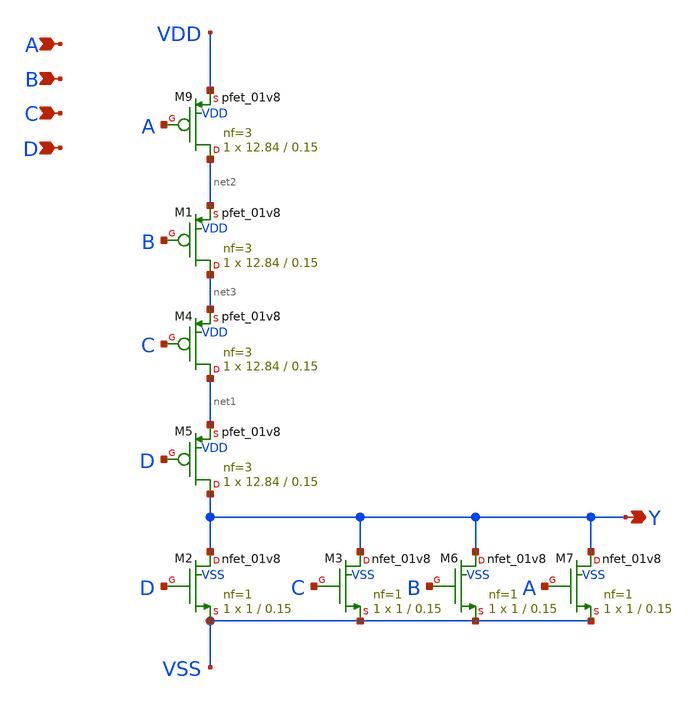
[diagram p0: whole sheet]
** sch_path: design/xschem/NOR/nor4.sch
**.subckt nor4 Y B C A D
*.opin Y
*.ipin B
*.ipin C
*.ipin A
*.ipin D
XM2 Y D VSS VSS sky130_fd_pr__nfet_01v8 L=0.15 W=1 nf=1 ad='int((nf+1)/2) * W/nf * 0.29' as='int((nf+2)/2) * W/nf * 0.29'
+ pd='2*int((nf+1)/2) * (W/nf + 0.29)' ps='2*int((nf+2)/2) * (W/nf + 0.29)' nrd='0.29 / W' nrs='0.29 / W'
+ sa=0 sb=0 sd=0 mult=1 m=1
XM3 Y C VSS VSS sky130_fd_pr__nfet_01v8 L=0.15 W=1 nf=1 ad='int((nf+1)/2) * W/nf * 0.29' as='int((nf+2)/2) * W/nf * 0.29'
+ pd='2*int((nf+1)/2) * (W/nf + 0.29)' ps='2*int((nf+2)/2) * (W/nf + 0.29)' nrd='0.29 / W' nrs='0.29 / W'
+ sa=0 sb=0 sd=0 mult=1 m=1
XM6 Y B VSS VSS sky130_fd_pr__nfet_01v8 L=0.15 W=1 nf=1 ad='int((nf+1)/2) * W/nf * 0.29' as='int((nf+2)/2) * W/nf * 0.29'
+ pd='2*int((nf+1)/2) * (W/nf + 0.29)' ps='2*int((nf+2)/2) * (W/nf + 0.29)' nrd='0.29 / W' nrs='0.29 / W'
+ sa=0 sb=0 sd=0 mult=1 m=1
XM7 Y A VSS VSS sky130_fd_pr__nfet_01v8 L=0.15 W=1 nf=1 ad='int((nf+1)/2) * W/nf * 0.29' as='int((nf+2)/2) * W/nf * 0.29'
+ pd='2*int((nf+1)/2) * (W/nf + 0.29)' ps='2*int((nf+2)/2) * (W/nf + 0.29)' nrd='0.29 / W' nrs='0.29 / W'
+ sa=0 sb=0 sd=0 mult=1 m=1
XM9 net2 A VDD VDD sky130_fd_pr__pfet_01v8 L=0.15 W=12.84 nf=3 ad='int((nf+1)/2) * W/nf * 0.29' as='int((nf+2)/2) * W/nf * 0.29'
+ pd='2*int((nf+1)/2) * (W/nf + 0.29)' ps='2*int((nf+2)/2) * (W/nf + 0.29)' nrd='0.29 / W' nrs='0.29 / W'
+ sa=0 sb=0 sd=0 mult=1 m=1
XM1 net3 B net2 VDD sky130_fd_pr__pfet_01v8 L=0.15 W=12.84 nf=3 ad='int((nf+1)/2) * W/nf * 0.29' as='int((nf+2)/2) * W/nf * 0.29'
+ pd='2*int((nf+1)/2) * (W/nf + 0.29)' ps='2*int((nf+2)/2) * (W/nf + 0.29)' nrd='0.29 / W' nrs='0.29 / W'
+ sa=0 sb=0 sd=0 mult=1 m=1
XM4 net1 C net3 VDD sky130_fd_pr__pfet_01v8 L=0.15 W=12.84 nf=3 ad='int((nf+1)/2) * W/nf * 0.29' as='int((nf+2)/2) * W/nf * 0.29'
+ pd='2*int((nf+1)/2) * (W/nf + 0.29)' ps='2*int((nf+2)/2) * (W/nf + 0.29)' nrd='0.29 / W' nrs='0.29 / W'
+ sa=0 sb=0 sd=0 mult=1 m=1
XM5 Y D net1 VDD sky130_fd_pr__pfet_01v8 L=0.15 W=12.84 nf=3 ad='int((nf+1)/2) * W/nf * 0.29' as='int((nf+2)/2) * W/nf * 0.29'
+ pd='2*int((nf+1)/2) * (W/nf + 0.29)' ps='2*int((nf+2)/2) * (W/nf + 0.29)' nrd='0.29 / W' nrs='0.29 / W'
+ sa=0 sb=0 sd=0 mult=1 m=1
**.ends
.end
